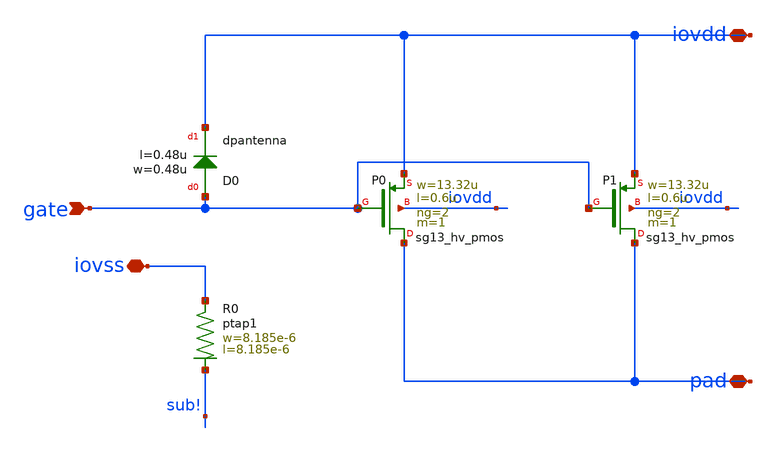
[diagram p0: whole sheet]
** sch_path: ihp-sg13g2/libs.ref/sg13g2_io/sch/xschem/sg13g2_Clamp_P2N2D.sch
**.subckt sg13g2_Clamp_P2N2D iovdd iovss pad gate
*.iopin iovdd
*.iopin iovss
*.iopin pad
*.ipin gate
XP0 pad gate iovdd iovdd sg13_hv_pmos w=13.32u l=0.6u ng=2 m=1 mm_ok=1
XP1 pad gate iovdd iovdd sg13_hv_pmos w=13.32u l=0.6u ng=2 m=1 mm_ok=1
XD0 gate iovdd dpantenna l=0.48u w=0.48u
XR0 iovss sub! ptap1 R=9.826 w=8.185e-6 l=8.185e-6
**.ends
.end
